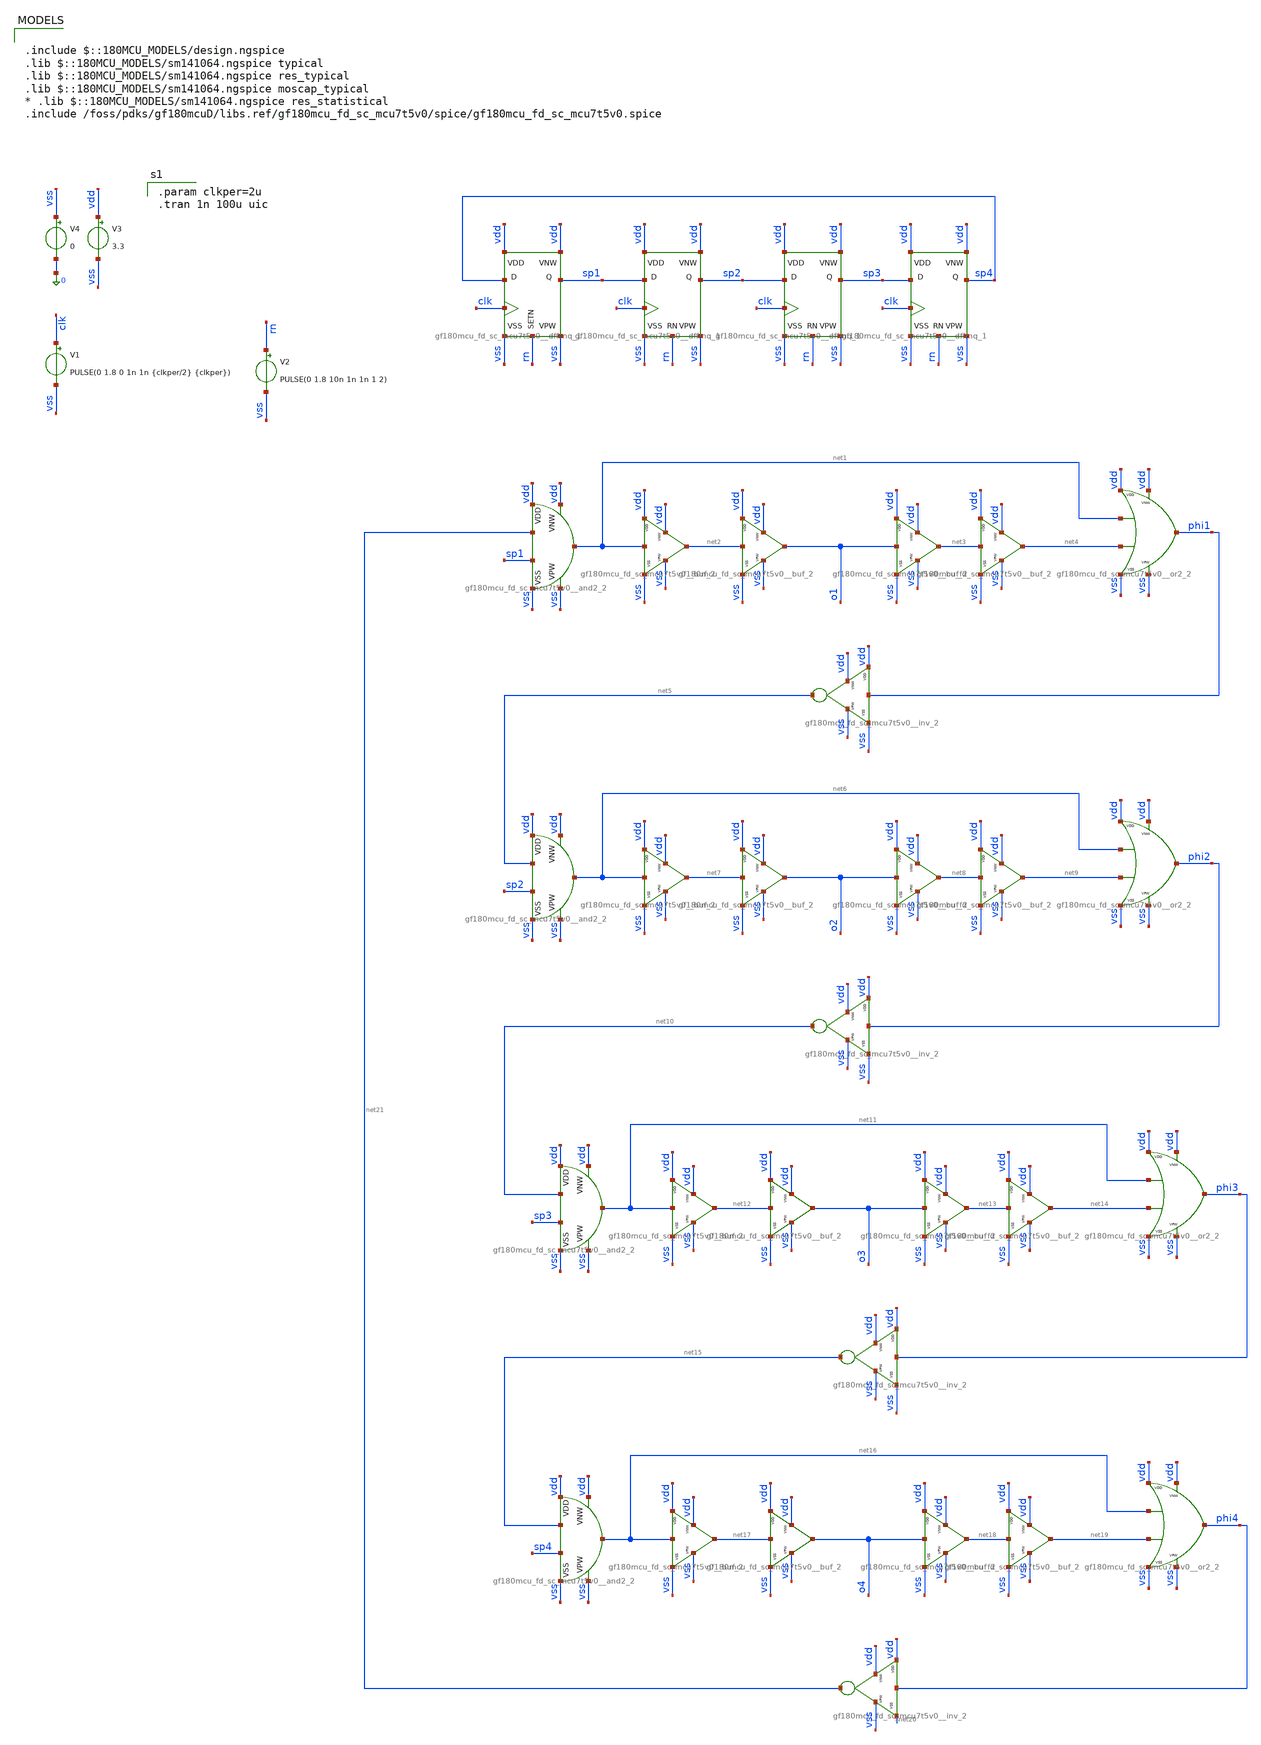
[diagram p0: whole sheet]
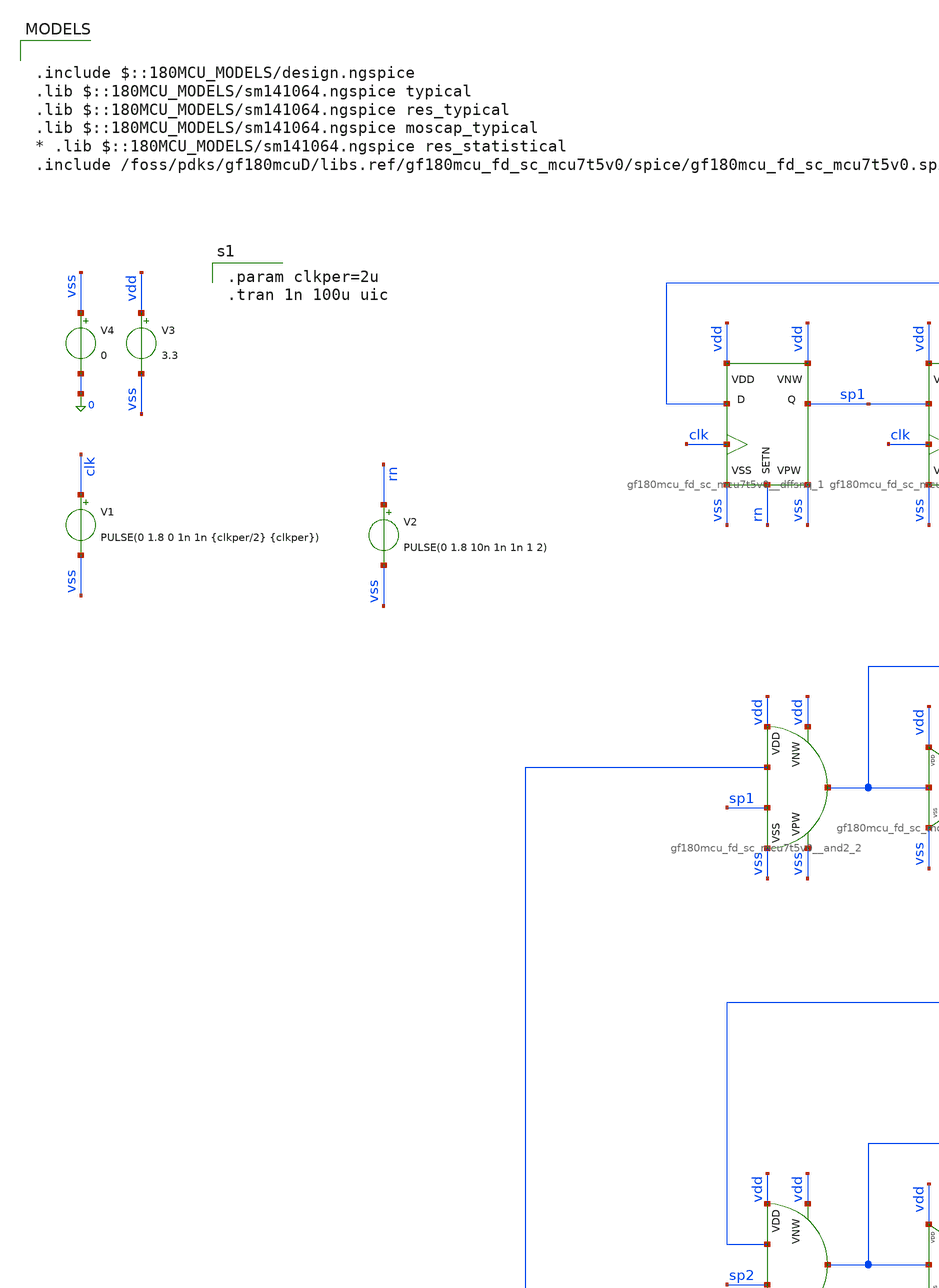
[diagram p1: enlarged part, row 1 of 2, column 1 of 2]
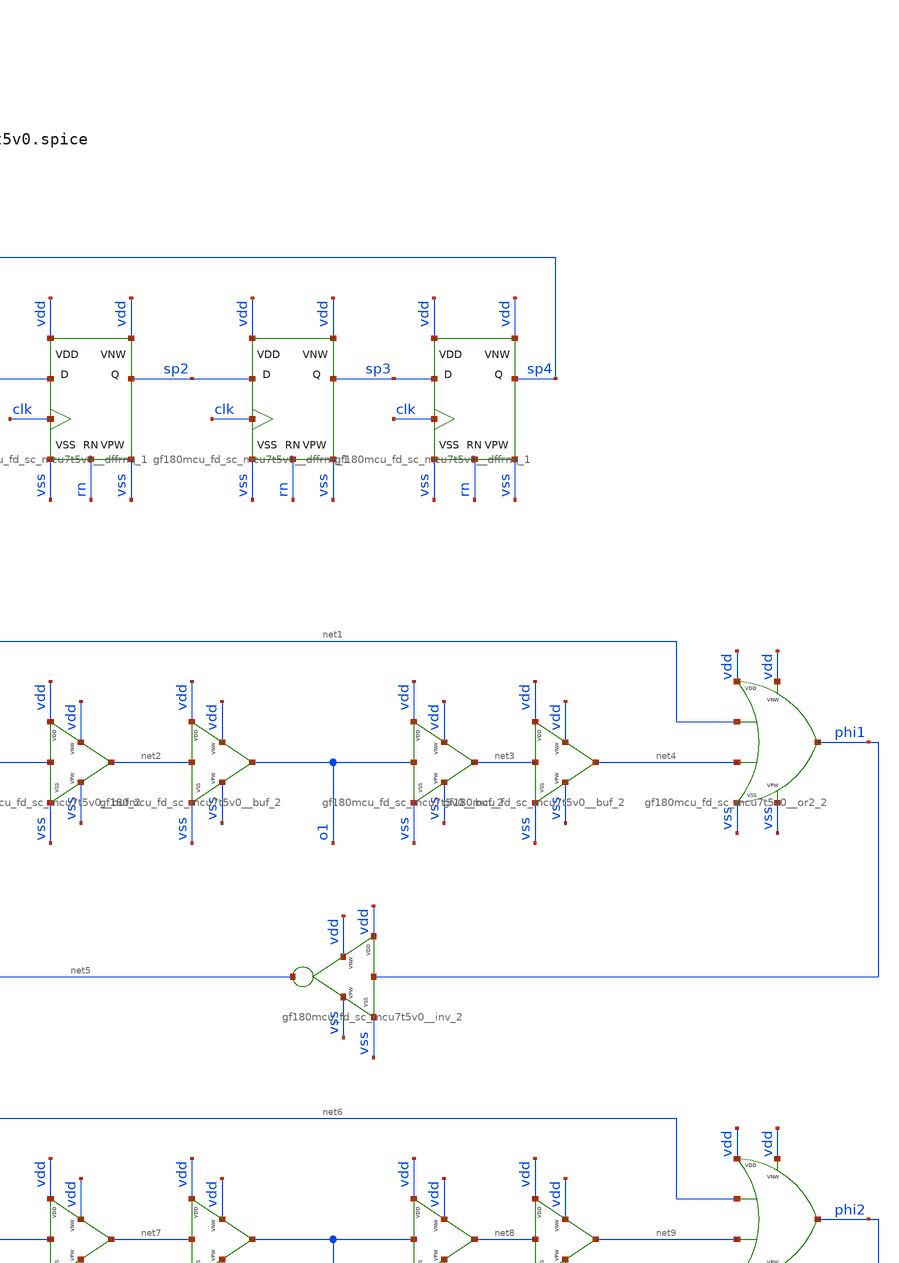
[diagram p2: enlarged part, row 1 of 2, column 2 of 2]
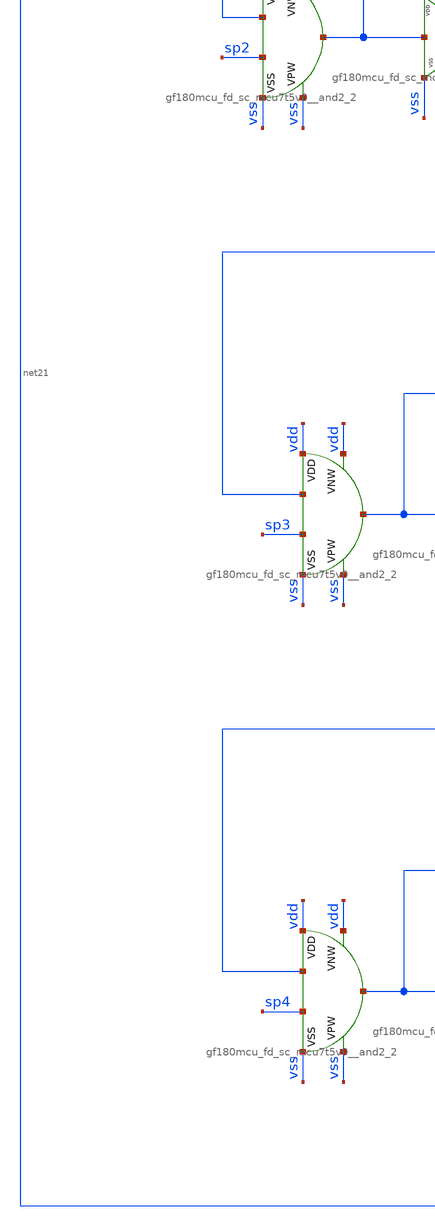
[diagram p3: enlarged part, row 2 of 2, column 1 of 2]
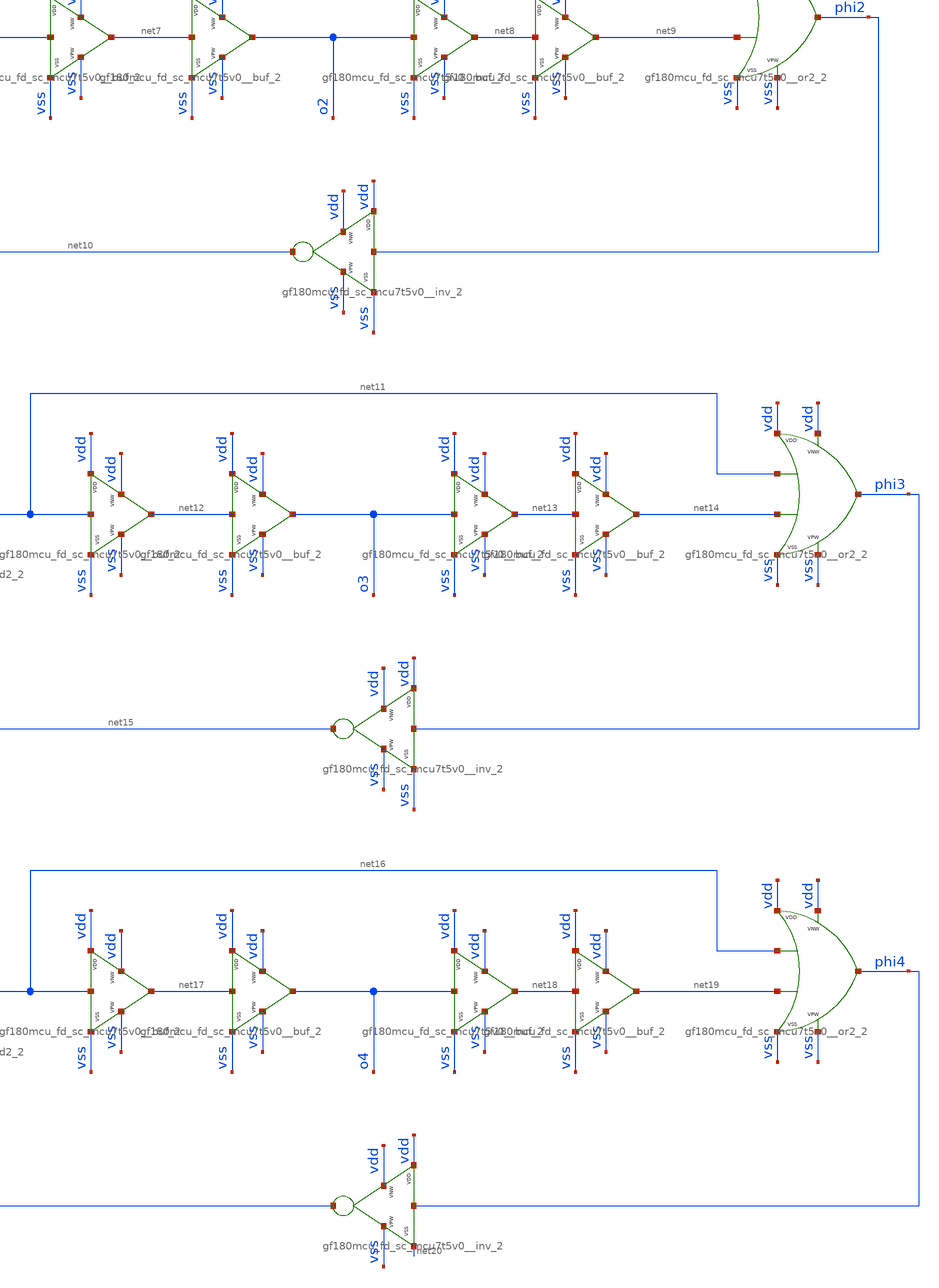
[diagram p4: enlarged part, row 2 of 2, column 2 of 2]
** sch_path: xschem/clk_gen/clk_gen_test.sch
**.subckt clk_gen_test
x1 sp4 rn clk sp1 vdd vdd vss vss gf180mcu_fd_sc_mcu7t5v0__dffsnq_1
x2 sp1 rn clk sp2 vdd vdd vss vss gf180mcu_fd_sc_mcu7t5v0__dffrnq_1
x3 sp2 rn clk sp3 vdd vdd vss vss gf180mcu_fd_sc_mcu7t5v0__dffrnq_1
x4 sp3 rn clk sp4 vdd vdd vss vss gf180mcu_fd_sc_mcu7t5v0__dffrnq_1
V1 clk vss PULSE(0 1.8 0 1n 1n {clkper/2} {clkper})
V3 vdd vss 3.3
V4 vss 0 0
V2 rn vss PULSE(0 1.8 10n 1n 1n 1 2)
x5 net21 sp1 net1 vdd vdd vss vss gf180mcu_fd_sc_mcu7t5v0__and2_2
x6 phi1 net5 vdd vdd vss vss gf180mcu_fd_sc_mcu7t5v0__inv_2
x7 net5 sp2 net6 vdd vdd vss vss gf180mcu_fd_sc_mcu7t5v0__and2_2
x8 phi2 net10 vdd vdd vss vss gf180mcu_fd_sc_mcu7t5v0__inv_2
x9 net10 sp3 net11 vdd vdd vss vss gf180mcu_fd_sc_mcu7t5v0__and2_2
x10 phi3 net15 vdd vdd vss vss gf180mcu_fd_sc_mcu7t5v0__inv_2
x11 net15 sp4 net16 vdd vdd vss vss gf180mcu_fd_sc_mcu7t5v0__and2_2
x12 phi4 net21 vdd vdd vss net20 gf180mcu_fd_sc_mcu7t5v0__inv_2
x13 net1 net2 vdd vdd vss vss gf180mcu_fd_sc_mcu7t5v0__buf_2
x14 net2 o1 vdd vdd vss vss gf180mcu_fd_sc_mcu7t5v0__buf_2
x15 o1 net3 vdd vdd vss vss gf180mcu_fd_sc_mcu7t5v0__buf_2
x16 net3 net4 vdd vdd vss vss gf180mcu_fd_sc_mcu7t5v0__buf_2
x17 net6 net7 vdd vdd vss vss gf180mcu_fd_sc_mcu7t5v0__buf_2
x18 net7 o2 vdd vdd vss vss gf180mcu_fd_sc_mcu7t5v0__buf_2
x19 o2 net8 vdd vdd vss vss gf180mcu_fd_sc_mcu7t5v0__buf_2
x20 net8 net9 vdd vdd vss vss gf180mcu_fd_sc_mcu7t5v0__buf_2
x21 net11 net12 vdd vdd vss vss gf180mcu_fd_sc_mcu7t5v0__buf_2
x22 net12 o3 vdd vdd vss vss gf180mcu_fd_sc_mcu7t5v0__buf_2
x23 o3 net13 vdd vdd vss vss gf180mcu_fd_sc_mcu7t5v0__buf_2
x24 net13 net14 vdd vdd vss vss gf180mcu_fd_sc_mcu7t5v0__buf_2
x25 net16 net17 vdd vdd vss vss gf180mcu_fd_sc_mcu7t5v0__buf_2
x26 net17 o4 vdd vdd vss vss gf180mcu_fd_sc_mcu7t5v0__buf_2
x27 o4 net18 vdd vdd vss vss gf180mcu_fd_sc_mcu7t5v0__buf_2
x28 net18 net19 vdd vdd vss vss gf180mcu_fd_sc_mcu7t5v0__buf_2
x29 net16 net19 phi4 vdd vdd vss vss gf180mcu_fd_sc_mcu7t5v0__or2_2
x30 net11 net14 phi3 vdd vdd vss vss gf180mcu_fd_sc_mcu7t5v0__or2_2
x31 net6 net9 phi2 vdd vdd vss vss gf180mcu_fd_sc_mcu7t5v0__or2_2
x32 net1 net4 phi1 vdd vdd vss vss gf180mcu_fd_sc_mcu7t5v0__or2_2
**** begin user architecture code

.param clkper=2u
.tran 1n 100u uic


.include $::180MCU_MODELS/design.ngspice
.lib $::180MCU_MODELS/sm141064.ngspice typical
.lib $::180MCU_MODELS/sm141064.ngspice res_typical
.lib $::180MCU_MODELS/sm141064.ngspice moscap_typical
* .lib $::180MCU_MODELS/sm141064.ngspice res_statistical
.include /foss/pdks/gf180mcuD/libs.ref/gf180mcu_fd_sc_mcu7t5v0/spice/gf180mcu_fd_sc_mcu7t5v0.spice

**** end user architecture code
**.ends
.end
